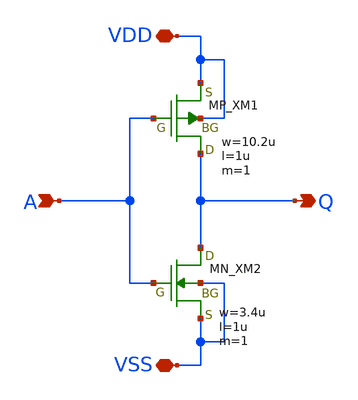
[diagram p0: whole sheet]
** sch_path: member_project/inverter_MUX/INV_03.sch
**.subckt INV_03 VSS A VDD Q
*.iopin VSS
*.ipin A
*.iopin VDD
*.opin Q
XM1 Q A VDD VDD PMOS w=10.2u l=1u as=0 ad=0 ps=0 pd=0 nrd=0 nrs=0 m=1
XM2 Q A VSS VSS NMOS w=3.4u l=1u as=0 ad=0 ps=0 pd=0 nrd=0 nrs=0 m=1
**.ends
.end
